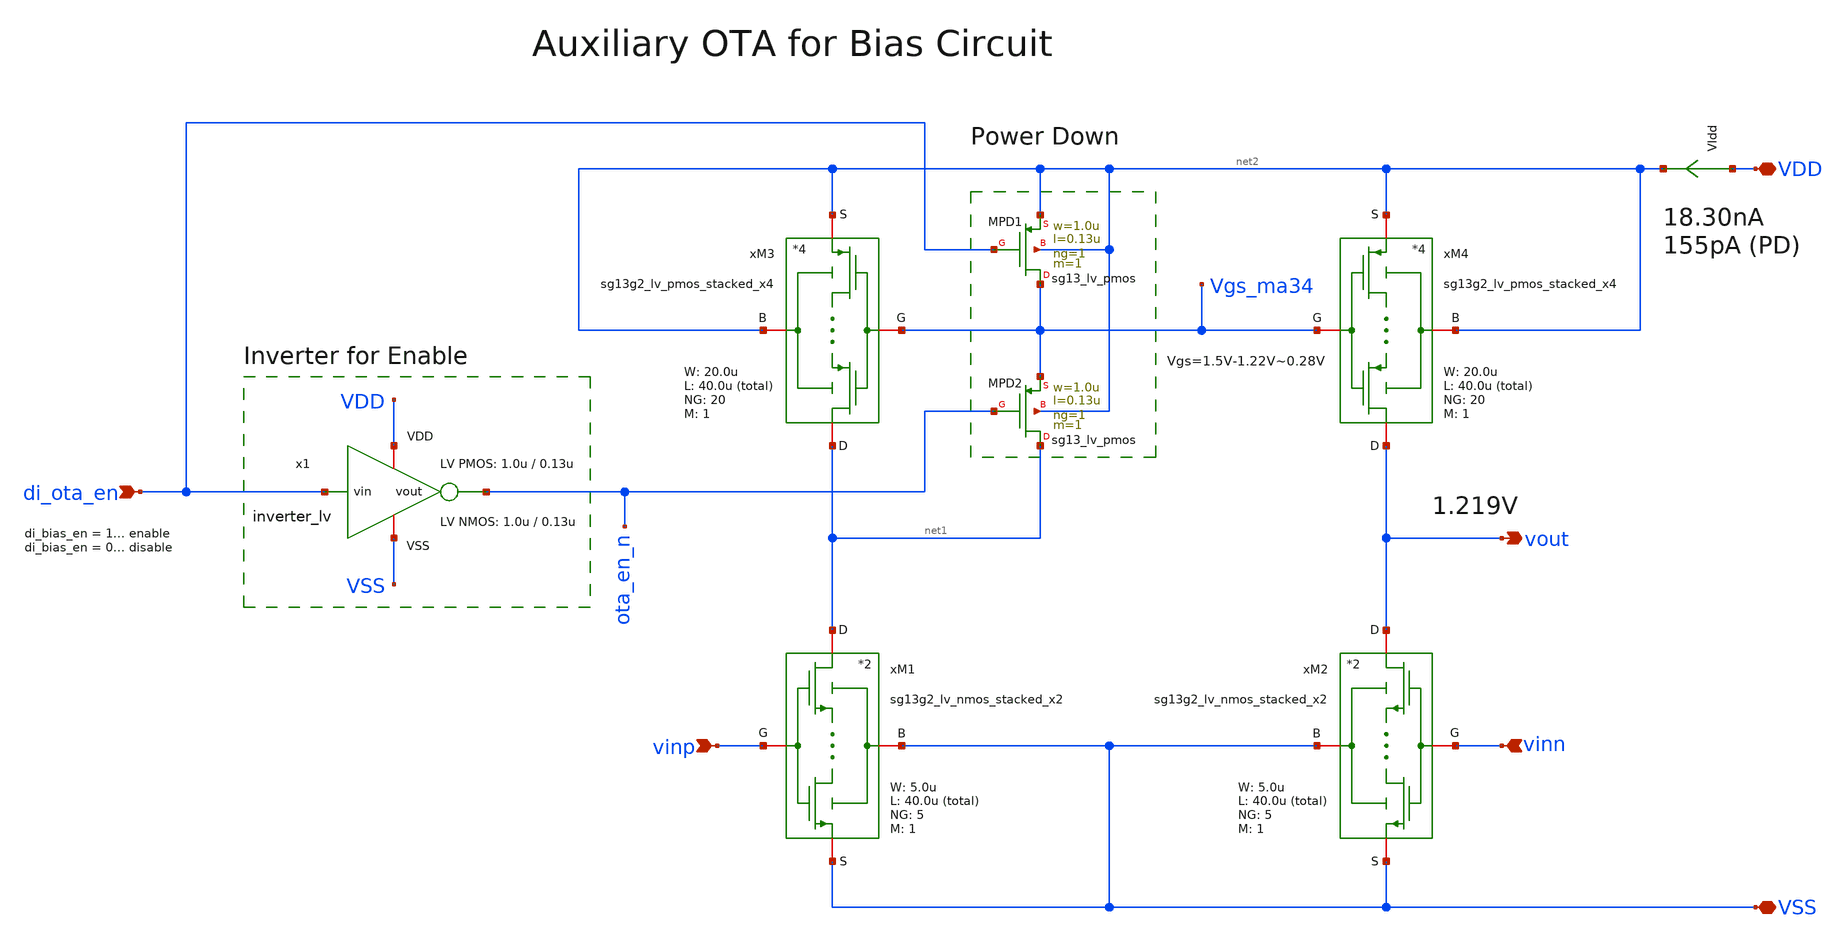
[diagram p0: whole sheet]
** sch_path: SG13G2_ATBS-ADC-main/xschem/bio_amplifier/amplifier_core/bias_circuit/aux_ota/aux_ota.sch
**.subckt aux_ota VDD VSS di_ota_en vinp vinn vout
*.iopin VDD
*.iopin VSS
*.ipin di_ota_en
*.ipin vinp
*.ipin vinn
*.opin vout
xM3 net1 Vgs_ma34 net2 net2 sg13g2_lv_pmos_stacked_x4 W_P=20.0u L_P=40.0u NG_P=20 M_P=1
xM4 vout Vgs_ma34 net2 net2 sg13g2_lv_pmos_stacked_x4 W_P=20.0u L_P=40.0u NG_P=20 M_P=1
xM1 net1 vinp VSS VSS sg13g2_lv_nmos_stacked_x2 W_N=5.0u L_N=40.0u NG_N=5 M_N=1
VIdd VDD net2 0
.save i(vidd)
xM2 vout vinn VSS VSS sg13g2_lv_nmos_stacked_x2 W_N=5.0u L_N=40.0u NG_N=5 M_N=1
XMPD1 Vgs_ma34 di_ota_en net2 net2 sg13_lv_pmos w=1.0u l=0.13u ng=1 m=1 mm_ok=1
XMPD2 net1 ota_en_n Vgs_ma34 net2 sg13_lv_pmos w=1.0u l=0.13u ng=1 m=1 mm_ok=1
x1 VDD di_ota_en ota_en_n VSS inverter_lv W_P=1.0u L_P=0.13u W_N=1.0u L_N=0.13u
**.ends

* expanding   symbol:  stacked_transistors/sg13g2_lv_pmos_stacked/sg13g2_lv_pmos_stacked_x4.sym # of
*+ pins=4
** sym_path: SG13G2_ATBS-ADC-main/xschem/stacked_transistors/sg13g2_lv_pmos_stacked/sg13g2_lv_pmos_stacked_x4.sym
** sch_path: SG13G2_ATBS-ADC-main/xschem/stacked_transistors/sg13g2_lv_pmos_stacked/sg13g2_lv_pmos_stacked_x4.sch
.subckt sg13g2_lv_pmos_stacked_x4 D G B S  W_P=1.0u L_P=0.45u NG_P=1 M_P=1
*.iopin D
*.iopin S
*.iopin G
*.iopin B
XM1 net1 G S B sg13_lv_pmos w=W_P l=L_P/4 ng=NG_P m=M_P mm_ok=1
XM2 net3 G net1 B sg13_lv_pmos w=W_P l=L_P/4 ng=NG_P m=M_P mm_ok=1
XM3 net2 G net3 B sg13_lv_pmos w=W_P l=L_P/4 ng=NG_P m=M_P mm_ok=1
XM4 D G net2 B sg13_lv_pmos w=W_P l=L_P/4 ng=NG_P m=M_P mm_ok=1
.ends


* expanding   symbol:  stacked_transistors/sg13g2_lv_nmos_stacked/sg13g2_lv_nmos_stacked_x2.sym # of
*+ pins=4
** sym_path: SG13G2_ATBS-ADC-main/xschem/stacked_transistors/sg13g2_lv_nmos_stacked/sg13g2_lv_nmos_stacked_x2.sym
** sch_path: SG13G2_ATBS-ADC-main/xschem/stacked_transistors/sg13g2_lv_nmos_stacked/sg13g2_lv_nmos_stacked_x2.sch
.subckt sg13g2_lv_nmos_stacked_x2 D G B S  W_N=1.0u L_N=0.45u NG_N=1 M_N=1
*.iopin D
*.iopin S
*.iopin G
*.iopin B
XM1 net1 G S B sg13_lv_nmos w=W_N l=L_N/2 ng=NG_N m=M_N mm_ok=1
XM2 D G net1 B sg13_lv_nmos w=W_N l=L_N/2 ng=NG_N m=M_N mm_ok=1
.ends


* expanding   symbol:  inverter/inverter_lv.sym # of pins=4
** sym_path: SG13G2_ATBS-ADC-main/xschem/inverter/inverter_lv.sym
** sch_path: SG13G2_ATBS-ADC-main/xschem/inverter/inverter_lv.sch
.subckt inverter_lv VDD vin vout VSS  W_P=3.0u L_P=0.13u W_N=1.0u L_N=0.13u
*.ipin vin
*.iopin VDD
*.iopin VSS
*.opin vout
XM1 vout vin VDD VDD sg13_lv_pmos w=W_P l=L_P ng=1 m=1 mm_ok=1
XM2 vout vin VSS VSS sg13_lv_nmos w=W_N l=L_N ng=1 m=1 mm_ok=1
.ends

.end
